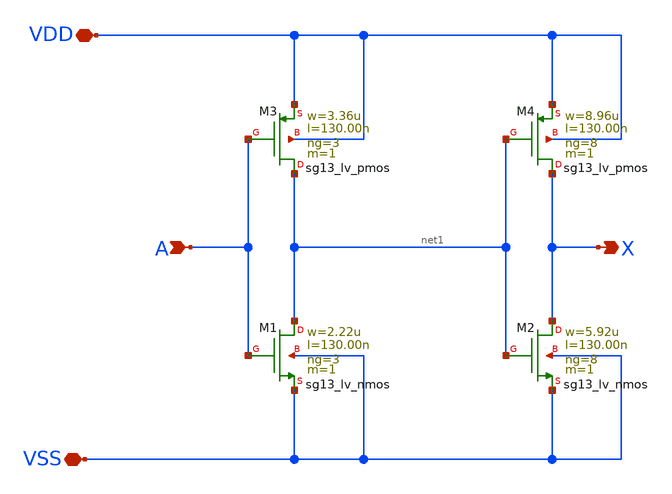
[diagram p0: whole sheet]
** sch_path: ihp-sg13g2/libs.tech/xschem/sg13g2_stdcells/sg13g2_buf_8.sch
* Copyright 2023 IHP PDK Authors
* Licensed under the Apache License, Version 2.0 (the "License");
* you may not use this file except in compliance with the License.
* You may obtain a copy of the License at
* https://www.apache.org/licenses/LICENSE-2.0
* Unless required by applicable law or agreed to in writing, software
* distributed under the License is distributed on an "AS IS" BASIS,
* WITHOUT WARRANTIES OR CONDITIONS OF ANY KIND, either express or implied.
* See the License for the specific language governing permissions and
* limitations under the License.
**.subckt sg13g2_buf_8 A X VDD VSS
*.ipin A
*.opin X
*.iopin VDD
*.iopin VSS
XM1 net1 A VSS VSS sg13_lv_nmos w=2.22u l=130.00n ng=3 m=1 mm_ok=1
XM2 X net1 VSS VSS sg13_lv_nmos w=5.92u l=130.00n ng=8 m=1 mm_ok=1
XM3 net1 A VDD VDD sg13_lv_pmos w=3.36u l=130.00n ng=3 m=1 mm_ok=1
XM4 X net1 VDD VDD sg13_lv_pmos w=8.96u l=130.00n ng=8 m=1 mm_ok=1
**.ends
.end
